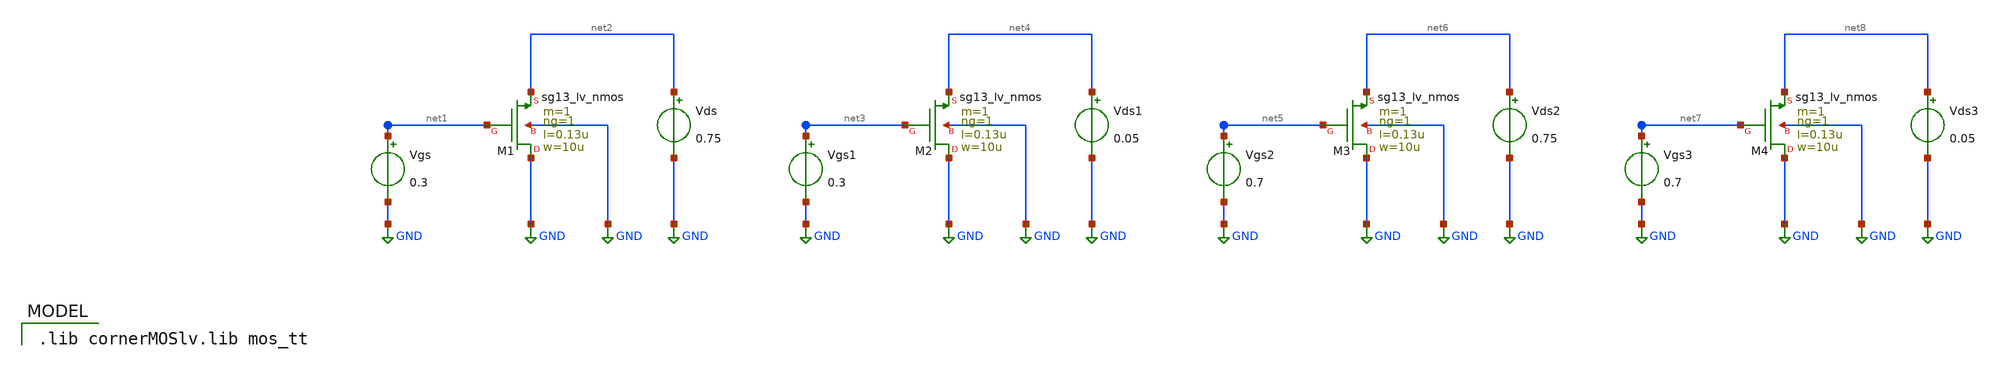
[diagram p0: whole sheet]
** sch_path: xschem/ex01.sch
* (c) 2024 H. Pretl, Apache-2.0 license
**.subckt ex01
Vgs net1 GND 0.3
Vds net2 GND 0.75
XM1 GND net1 net2 GND sg13_lv_nmos w=10u l=0.13u ng=1 m=1 mm_ok=1
Vgs1 net3 GND 0.3
Vds1 net4 GND 0.05
XM2 GND net3 net4 GND sg13_lv_nmos w=10u l=0.13u ng=1 m=1 mm_ok=1
Vgs2 net5 GND 0.7
Vds2 net6 GND 0.75
XM3 GND net5 net6 GND sg13_lv_nmos w=10u l=0.13u ng=1 m=1 mm_ok=1
Vgs3 net7 GND 0.7
Vds3 net8 GND 0.05
XM4 GND net7 net8 GND sg13_lv_nmos w=10u l=0.13u ng=1 m=1 mm_ok=1
**** begin user architecture code
 .lib cornerMOSlv.lib mos_tt



.temp 27
.control
save all

save @n.xm1.nsg13_lv_nmos[ids]
save @n.xm1.nsg13_lv_nmos[gm]
save @n.xm1.nsg13_lv_nmos[gmb]
save @n.xm1.nsg13_lv_nmos[gds]
save @n.xm1.nsg13_lv_nmos[cgg]
save @n.xm1.nsg13_lv_nmos[cgd]
save @n.xm1.nsg13_lv_nmos[cgs]
save @n.xm1.nsg13_lv_nmos[cgb]
save @n.xm1.nsg13_lv_nmos[fug]
save @n.xm1.nsg13_lv_nmos[sid]

save @n.xm2.nsg13_lv_nmos[ids]
save @n.xm2.nsg13_lv_nmos[gm]
save @n.xm2.nsg13_lv_nmos[gmb]
save @n.xm2.nsg13_lv_nmos[gds]
save @n.xm2.nsg13_lv_nmos[cgg]
save @n.xm2.nsg13_lv_nmos[cgd]
save @n.xm2.nsg13_lv_nmos[cgs]
save @n.xm2.nsg13_lv_nmos[cgb]
save @n.xm2.nsg13_lv_nmos[fug]
save @n.xm2.nsg13_lv_nmos[sid]

save @n.xm3.nsg13_lv_nmos[ids]
save @n.xm3.nsg13_lv_nmos[gm]
save @n.xm3.nsg13_lv_nmos[gmb]
save @n.xm3.nsg13_lv_nmos[gds]
save @n.xm3.nsg13_lv_nmos[cgg]
save @n.xm3.nsg13_lv_nmos[cgd]
save @n.xm3.nsg13_lv_nmos[cgs]
save @n.xm3.nsg13_lv_nmos[cgb]
save @n.xm3.nsg13_lv_nmos[fug]
save @n.xm3.nsg13_lv_nmos[sid]

save @n.xm4.nsg13_lv_nmos[ids]
save @n.xm4.nsg13_lv_nmos[gm]
save @n.xm4.nsg13_lv_nmos[gmb]
save @n.xm4.nsg13_lv_nmos[gds]
save @n.xm4.nsg13_lv_nmos[cgg]
save @n.xm4.nsg13_lv_nmos[cgd]
save @n.xm4.nsg13_lv_nmos[cgs]
save @n.xm4.nsg13_lv_nmos[cgb]
save @n.xm4.nsg13_lv_nmos[fug]
save @n.xm4.nsg13_lv_nmos[sid]

op
write ex01.raw
.endc


**** end user architecture code
**.ends
.GLOBAL GND
.end
